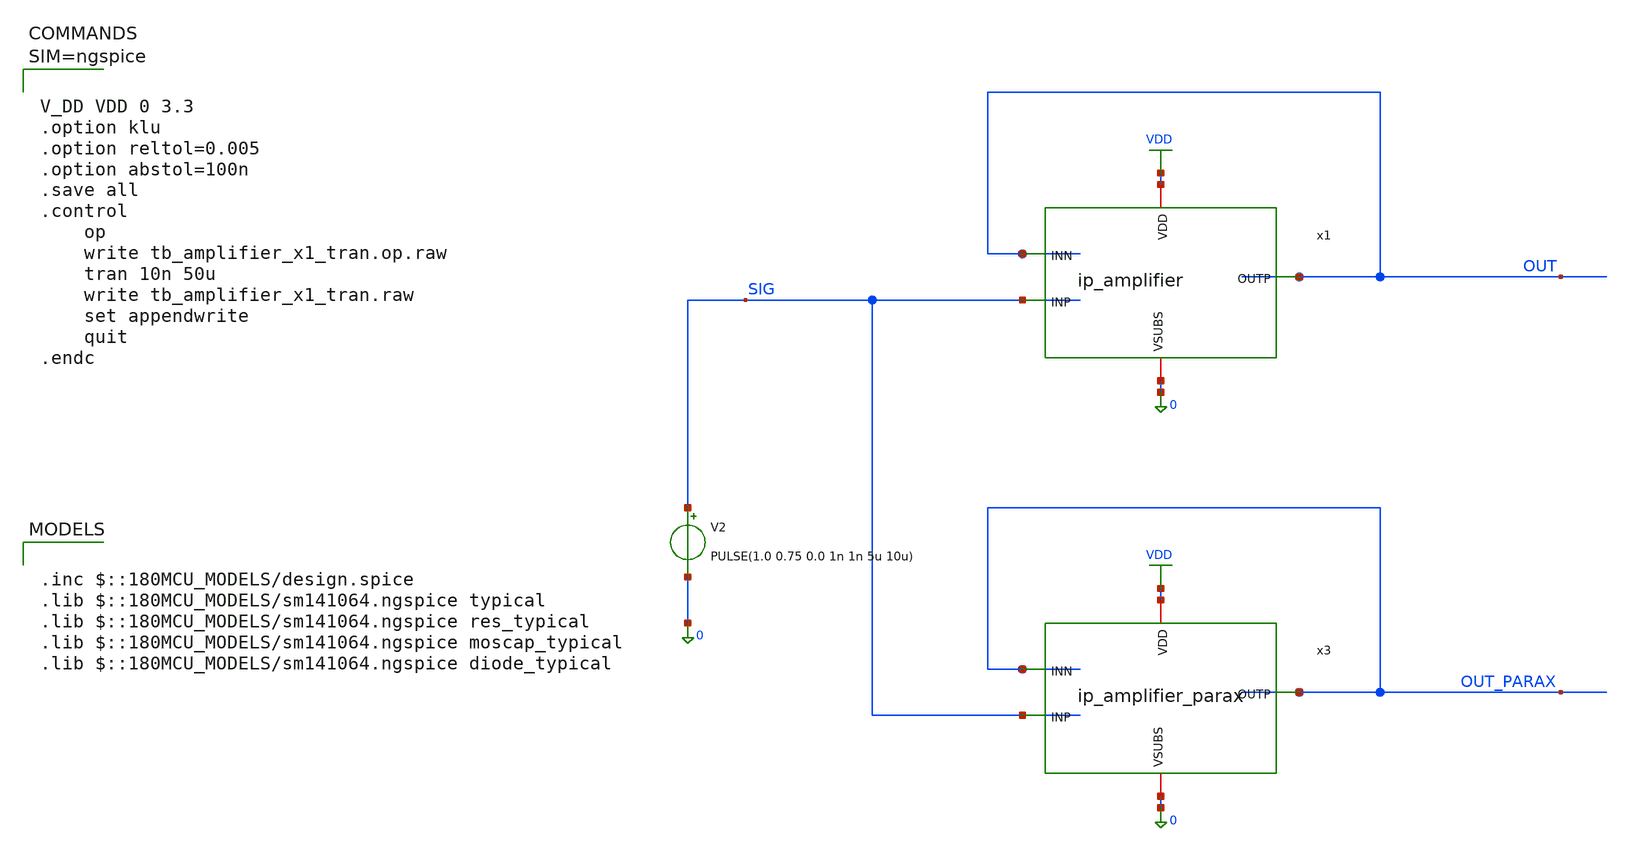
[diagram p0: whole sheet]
** sch_path: xschem/tb_amplifier_x1_tran.sch
**.subckt tb_amplifier_x1_tran
V2 SIG 0 PULSE(1.0 0.75 0.0 1n 1n 5u 10u)
x1 VDD OUT SIG OUT 0 ip_amplifier
x3 VDD OUT_PARAX SIG OUT_PARAX 0 ip_amplifier_parax
**** begin user architecture code

.inc $::180MCU_MODELS/design.spice
.lib $::180MCU_MODELS/sm141064.ngspice typical
.lib $::180MCU_MODELS/sm141064.ngspice res_typical
.lib $::180MCU_MODELS/sm141064.ngspice moscap_typical
.lib $::180MCU_MODELS/sm141064.ngspice diode_typical




V_DD VDD 0 3.3
.option klu
.option reltol=0.005
.option abstol=100n
.save all
.control
	op
	write tb_amplifier_x1_tran.op.raw
	tran 10n 50u
	write tb_amplifier_x1_tran.raw
	set appendwrite
	quit
.endc



**** end user architecture code
**.ends

* expanding   symbol:  ip_amplifier.sym # of pins=5
** sym_path: xschem/ip_amplifier.sym
** sch_path: xschem/ip_amplifier.sch
.subckt ip_amplifier VDD OUTP INP INN VSUBS
*.iopin VDD
*.iopin VSUBS
*.ipin INP
*.ipin INN
*.opin OUTP
XM1 COMP INP COMMON_ VDD pfet_03v3 L=5u W=18.0u nf=1 ad='int((nf+1)/2) * W/nf * 0.18u' as='int((nf+2)/2) * W/nf * 0.18u'
+ pd='2*int((nf+1)/2) * (W/nf + 0.18u)' ps='2*int((nf+2)/2) * (W/nf + 0.18u)' nrd='0.18u / W' nrs='0.18u / W'
+ sa=0 sb=0 sd=0 m=1 par=1
XM2 net6 INN COMMON_ VDD pfet_03v3 L=5u W=18.0u nf=1 ad='int((nf+1)/2) * W/nf * 0.18u' as='int((nf+2)/2) * W/nf * 0.18u'
+ pd='2*int((nf+1)/2) * (W/nf + 0.18u)' ps='2*int((nf+2)/2) * (W/nf + 0.18u)' nrd='0.18u / W' nrs='0.18u / W'
+ sa=0 sb=0 sd=0 m=1 par=1
XM3 net2 NBIAS VSUBS vsubs nfet_03v3 L=2u W=6u nf=1 ad='int((nf+1)/2) * W/nf * 0.18u' as='int((nf+2)/2) * W/nf * 0.18u'
+ pd='2*int((nf+1)/2) * (W/nf + 0.18u)' ps='2*int((nf+2)/2) * (W/nf + 0.18u)' nrd='0.18u / W' nrs='0.18u / W'
+ sa=0 sb=0 sd=0 m=2 par=2
XM4 net1 NBIAS VSUBS vsubs nfet_03v3 L=2u W=6u nf=1 ad='int((nf+1)/2) * W/nf * 0.18u' as='int((nf+2)/2) * W/nf * 0.18u'
+ pd='2*int((nf+1)/2) * (W/nf + 0.18u)' ps='2*int((nf+2)/2) * (W/nf + 0.18u)' nrd='0.18u / W' nrs='0.18u / W'
+ sa=0 sb=0 sd=0 m=1 par=1
XM7 NBIAS NBIAS net2 vsubs nfet_03v3 L=0.5u W=6u nf=1 ad='int((nf+1)/2) * W/nf * 0.18u' as='int((nf+2)/2) * W/nf * 0.18u'
+ pd='2*int((nf+1)/2) * (W/nf + 0.18u)' ps='2*int((nf+2)/2) * (W/nf + 0.18u)' nrd='0.18u / W' nrs='0.18u / W'
+ sa=0 sb=0 sd=0 m=4 par=4
XM8 net3 NBIAS net1 vsubs nfet_03v3 L=0.5u W=6u nf=1 ad='int((nf+1)/2) * W/nf * 0.18u' as='int((nf+2)/2) * W/nf * 0.18u'
+ pd='2*int((nf+1)/2) * (W/nf + 0.18u)' ps='2*int((nf+2)/2) * (W/nf + 0.18u)' nrd='0.18u / W' nrs='0.18u / W'
+ sa=0 sb=0 sd=0 m=4 par=4
XM9 net4 PBIAS VDD VDD pfet_03v3 L=2u W=6u nf=1 ad='int((nf+1)/2) * W/nf * 0.18u' as='int((nf+2)/2) * W/nf * 0.18u'
+ pd='2*int((nf+1)/2) * (W/nf + 0.18u)' ps='2*int((nf+2)/2) * (W/nf + 0.18u)' nrd='0.18u / W' nrs='0.18u / W'
+ sa=0 sb=0 sd=0 m=1 par=1
XM10 net5 PBIAS VDD VDD pfet_03v3 L=2u W=6u nf=1 ad='int((nf+1)/2) * W/nf * 0.18u' as='int((nf+2)/2) * W/nf * 0.18u'
+ pd='2*int((nf+1)/2) * (W/nf + 0.18u)' ps='2*int((nf+2)/2) * (W/nf + 0.18u)' nrd='0.18u / W' nrs='0.18u / W'
+ sa=0 sb=0 sd=0 m=1 par=1
XM11 PBIAS PBIAS net4 VDD pfet_03v3 L=0.5u W=6u nf=1 ad='int((nf+1)/2) * W/nf * 0.18u' as='int((nf+2)/2) * W/nf * 0.18u'
+ pd='2*int((nf+1)/2) * (W/nf + 0.18u)' ps='2*int((nf+2)/2) * (W/nf + 0.18u)' nrd='0.18u / W' nrs='0.18u / W'
+ sa=0 sb=0 sd=0 m=4 par=4
XM12 COMMON PBIAS net5 VDD pfet_03v3 L=0.5u W=6u nf=1 ad='int((nf+1)/2) * W/nf * 0.18u' as='int((nf+2)/2) * W/nf * 0.18u'
+ pd='2*int((nf+1)/2) * (W/nf + 0.18u)' ps='2*int((nf+2)/2) * (W/nf + 0.18u)' nrd='0.18u / W' nrs='0.18u / W'
+ sa=0 sb=0 sd=0 m=4 par=4
XM13 COMP net6 VSUBS vsubs nfet_03v3 L=5u W=6u nf=1 ad='int((nf+1)/2) * W/nf * 0.18u' as='int((nf+2)/2) * W/nf * 0.18u'
+ pd='2*int((nf+1)/2) * (W/nf + 0.18u)' ps='2*int((nf+2)/2) * (W/nf + 0.18u)' nrd='0.18u / W' nrs='0.18u / W'
+ sa=0 sb=0 sd=0 m=1 par=1
XM14 net6 net6 VSUBS vsubs nfet_03v3 L=5u W=6u nf=1 ad='int((nf+1)/2) * W/nf * 0.18u' as='int((nf+2)/2) * W/nf * 0.18u'
+ pd='2*int((nf+1)/2) * (W/nf + 0.18u)' ps='2*int((nf+2)/2) * (W/nf + 0.18u)' nrd='0.18u / W' nrs='0.18u / W'
+ sa=0 sb=0 sd=0 m=1 par=1
XM17 net8 PBIAS VDD VDD pfet_03v3 L=0.5u W=12u nf=1 ad='int((nf+1)/2) * W/nf * 0.18u' as='int((nf+2)/2) * W/nf * 0.18u'
+ pd='2*int((nf+1)/2) * (W/nf + 0.18u)' ps='2*int((nf+2)/2) * (W/nf + 0.18u)' nrd='0.18u / W' nrs='0.18u / W'
+ sa=0 sb=0 sd=0 m=2 par=2
XM18 OUTP COMP VSUBS vsubs nfet_03v3 L=0.5u W=12u nf=1 ad='int((nf+1)/2) * W/nf * 0.18u' as='int((nf+2)/2) * W/nf * 0.18u'
+ pd='2*int((nf+1)/2) * (W/nf + 0.18u)' ps='2*int((nf+2)/2) * (W/nf + 0.18u)' nrd='0.18u / W' nrs='0.18u / W'
+ sa=0 sb=0 sd=0 m=4 par=4
XR3 NBIAS net7 vsubs ppolyf_u_1k r_width=1e-6 r_length=48e-6 m=1
Vmeas VDD net7 0
Vmeas1 PBIAS net3 0
XC1 OUTP net9 cap_pmos_03v3 c_width=13.5e-6 c_length=18e-6 m=1
XC2 COMP net9 cap_pmos_03v3 c_width=13.5e-6 c_length=18e-6 m=1
Vmeas2 COMMON COMMON_ 0
Vmeas3 net8 OUTP 0
XR2 VDD net9 vsubs ppolyf_u_1k r_width=1e-6 r_length=96e-6 m=1
.ends


* expanding   symbol:  ip_amplifier_parax.sym # of pins=5
** sym_path: xschem/ip_amplifier.sym
.include [file normalize ./parax/ip_amplifier.sim.spice]
.GLOBAL VDD
.end
